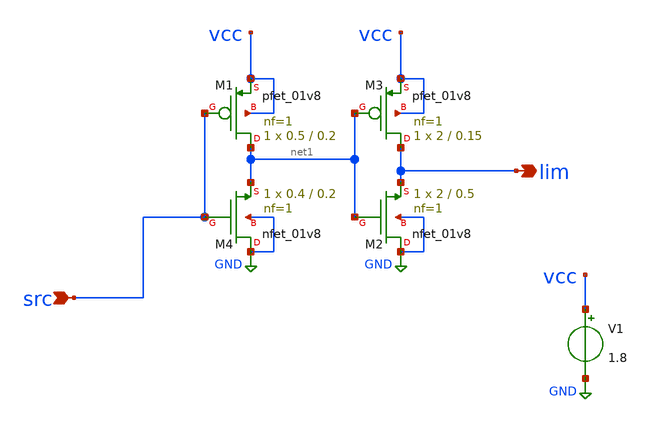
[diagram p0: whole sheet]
** sch_path: xschem/clim.sch
**.subckt clim src lim
*.ipin src
*.opin lim
XM4 GND src net1 GND sky130_fd_pr__nfet_01v8 L=0.2 W=0.4 nf=1 ad='int((nf+1)/2) * W/nf * 0.29' as='int((nf+2)/2) * W/nf * 0.29'
+ pd='2*int((nf+1)/2) * (W/nf + 0.29)' ps='2*int((nf+2)/2) * (W/nf + 0.29)' nrd='0.29 / W' nrs='0.29 / W'
+ sa=0 sb=0 sd=0 mult=1 m=1
V1 vcc GND 1.8
XM1 net1 src vcc vcc sky130_fd_pr__pfet_01v8 L=0.2 W=0.5 nf=1 ad='int((nf+1)/2) * W/nf * 0.29' as='int((nf+2)/2) * W/nf * 0.29'
+ pd='2*int((nf+1)/2) * (W/nf + 0.29)' ps='2*int((nf+2)/2) * (W/nf + 0.29)' nrd='0.29 / W' nrs='0.29 / W'
+ sa=0 sb=0 sd=0 mult=1 m=1
XM3 lim net1 vcc vcc sky130_fd_pr__pfet_01v8 L=0.15 W=2 nf=1 ad='int((nf+1)/2) * W/nf * 0.29' as='int((nf+2)/2) * W/nf * 0.29'
+ pd='2*int((nf+1)/2) * (W/nf + 0.29)' ps='2*int((nf+2)/2) * (W/nf + 0.29)' nrd='0.29 / W' nrs='0.29 / W'
+ sa=0 sb=0 sd=0 mult=1 m=1
XM2 GND net1 lim GND sky130_fd_pr__nfet_01v8 L=0.5 W=2 nf=1 ad='int((nf+1)/2) * W/nf * 0.29' as='int((nf+2)/2) * W/nf * 0.29'
+ pd='2*int((nf+1)/2) * (W/nf + 0.29)' ps='2*int((nf+2)/2) * (W/nf + 0.29)' nrd='0.29 / W' nrs='0.29 / W'
+ sa=0 sb=0 sd=0 mult=1 m=1
**.ends
.GLOBAL GND
.end
